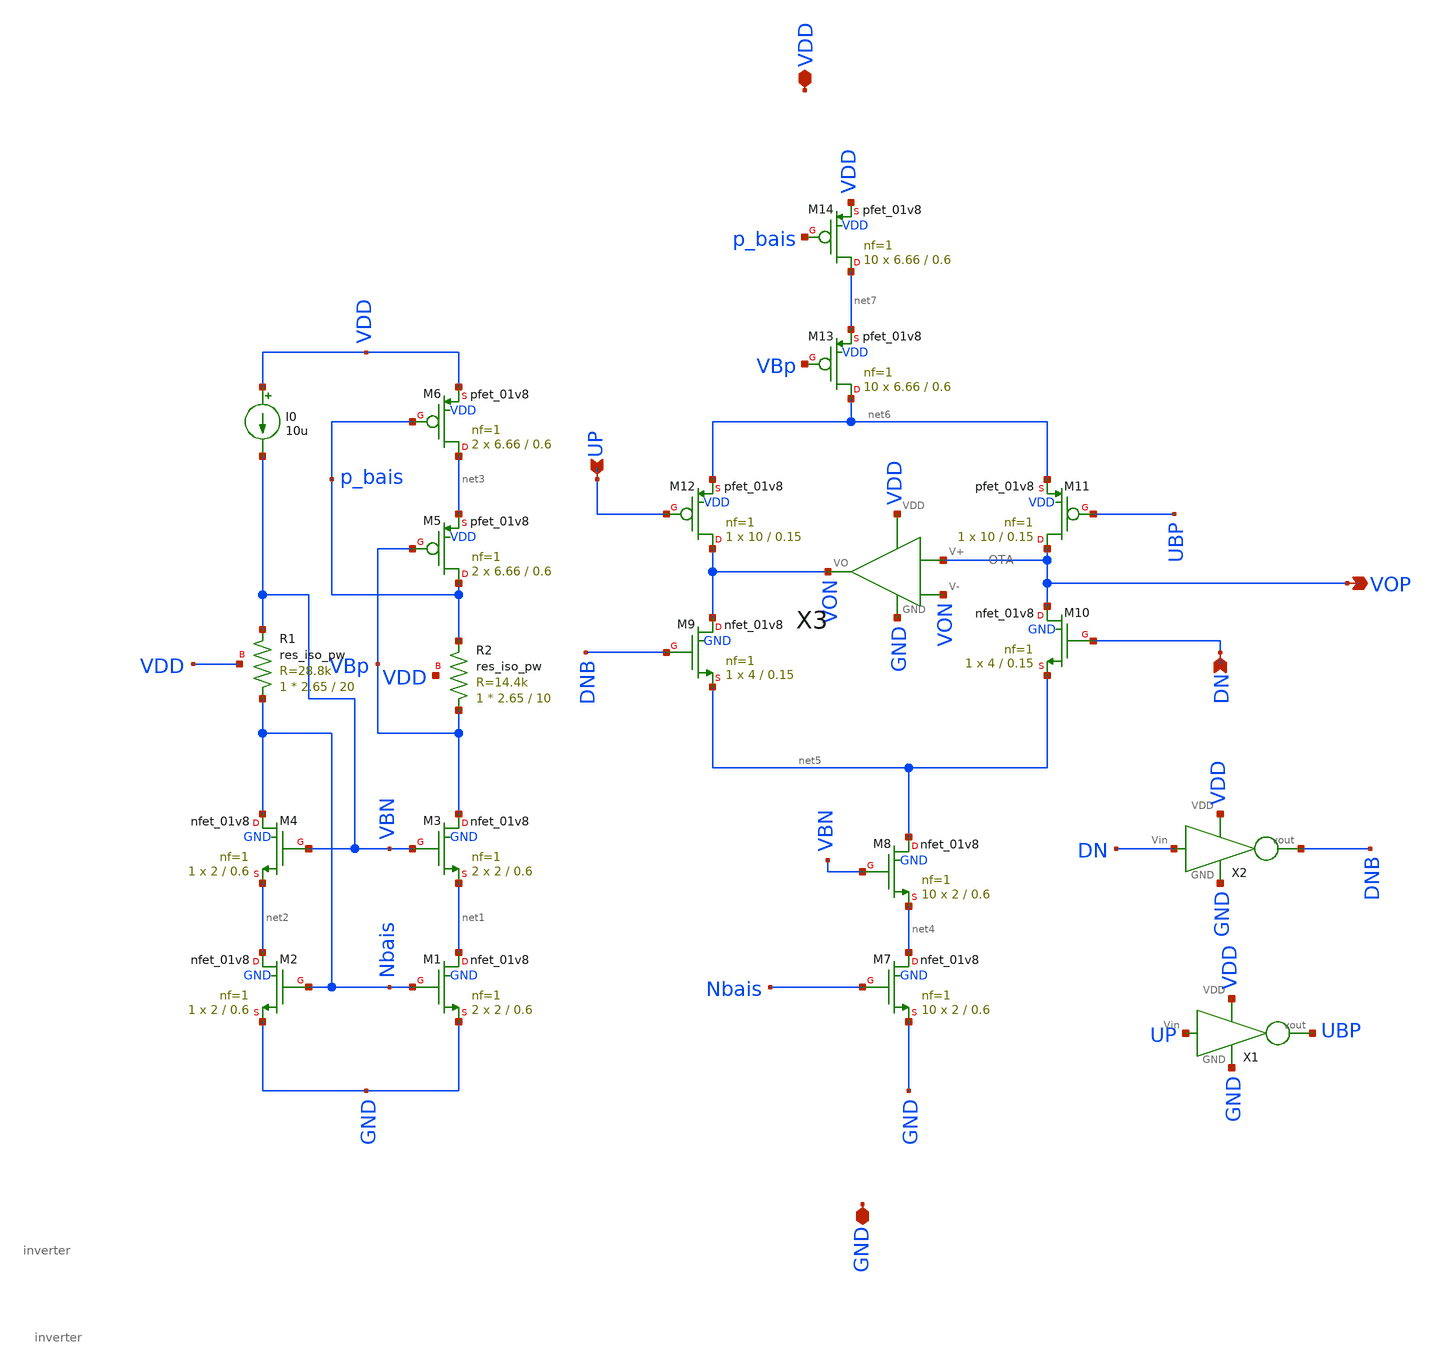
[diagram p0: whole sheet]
** sch_path: pll/pfd_cp_lf_lib/charge_pump_second_design/xschem/CP_with_buffer.sch
**.subckt CP_with_buffer VDD GND VOP DN UP
*.iopin VDD
*.iopin GND
*.opin VOP
*.ipin DN
*.ipin UP
XM1 net1 Nbais GND GND sky130_fd_pr__nfet_01v8 L=0.6 W=2 nf=1 ad='int((nf+1)/2) * W/nf * 0.29' as='int((nf+2)/2) * W/nf * 0.29'
+ pd='2*int((nf+1)/2) * (W/nf + 0.29)' ps='2*int((nf+2)/2) * (W/nf + 0.29)' nrd='0.29 / W' nrs='0.29 / W'
+ sa=0 sb=0 sd=0 mult=2 m=2
XM2 net2 Nbais GND GND sky130_fd_pr__nfet_01v8 L=0.6 W=2 nf=1 ad='int((nf+1)/2) * W/nf * 0.29' as='int((nf+2)/2) * W/nf * 0.29'
+ pd='2*int((nf+1)/2) * (W/nf + 0.29)' ps='2*int((nf+2)/2) * (W/nf + 0.29)' nrd='0.29 / W' nrs='0.29 / W'
+ sa=0 sb=0 sd=0 mult=1 m=1
XM3 VBp VBN net1 GND sky130_fd_pr__nfet_01v8 L=0.6 W=2 nf=1 ad='int((nf+1)/2) * W/nf * 0.29' as='int((nf+2)/2) * W/nf * 0.29'
+ pd='2*int((nf+1)/2) * (W/nf + 0.29)' ps='2*int((nf+2)/2) * (W/nf + 0.29)' nrd='0.29 / W' nrs='0.29 / W'
+ sa=0 sb=0 sd=0 mult=2 m=2
XM4 Nbais VBN net2 GND sky130_fd_pr__nfet_01v8 L=0.6 W=2 nf=1 ad='int((nf+1)/2) * W/nf * 0.29' as='int((nf+2)/2) * W/nf * 0.29'
+ pd='2*int((nf+1)/2) * (W/nf + 0.29)' ps='2*int((nf+2)/2) * (W/nf + 0.29)' nrd='0.29 / W' nrs='0.29 / W'
+ sa=0 sb=0 sd=0 mult=1 m=1
XM5 p_bais VBp net3 VDD sky130_fd_pr__pfet_01v8 L=0.6 W=6.66 nf=1 ad='int((nf+1)/2) * W/nf * 0.29' as='int((nf+2)/2) * W/nf * 0.29'
+ pd='2*int((nf+1)/2) * (W/nf + 0.29)' ps='2*int((nf+2)/2) * (W/nf + 0.29)' nrd='0.29 / W' nrs='0.29 / W'
+ sa=0 sb=0 sd=0 mult=2 m=2
XM6 net3 p_bais VDD VDD sky130_fd_pr__pfet_01v8 L=0.6 W=6.66 nf=1 ad='int((nf+1)/2) * W/nf * 0.29' as='int((nf+2)/2) * W/nf * 0.29'
+ pd='2*int((nf+1)/2) * (W/nf + 0.29)' ps='2*int((nf+2)/2) * (W/nf + 0.29)' nrd='0.29 / W' nrs='0.29 / W'
+ sa=0 sb=0 sd=0 mult=2 m=2
I0 VDD VBN 10u
XM7 net4 Nbais GND GND sky130_fd_pr__nfet_01v8 L=0.6 W=2 nf=1 ad='int((nf+1)/2) * W/nf * 0.29' as='int((nf+2)/2) * W/nf * 0.29'
+ pd='2*int((nf+1)/2) * (W/nf + 0.29)' ps='2*int((nf+2)/2) * (W/nf + 0.29)' nrd='0.29 / W' nrs='0.29 / W'
+ sa=0 sb=0 sd=0 mult=10 m=10
XM8 net5 VBN net4 GND sky130_fd_pr__nfet_01v8 L=0.6 W=2 nf=1 ad='int((nf+1)/2) * W/nf * 0.29' as='int((nf+2)/2) * W/nf * 0.29'
+ pd='2*int((nf+1)/2) * (W/nf + 0.29)' ps='2*int((nf+2)/2) * (W/nf + 0.29)' nrd='0.29 / W' nrs='0.29 / W'
+ sa=0 sb=0 sd=0 mult=10 m=10
XM9 VON DNB net5 GND sky130_fd_pr__nfet_01v8 L=0.15 W=4 nf=1 ad='int((nf+1)/2) * W/nf * 0.29' as='int((nf+2)/2) * W/nf * 0.29'
+ pd='2*int((nf+1)/2) * (W/nf + 0.29)' ps='2*int((nf+2)/2) * (W/nf + 0.29)' nrd='0.29 / W' nrs='0.29 / W'
+ sa=0 sb=0 sd=0 mult=1 m=1
XM10 VOP DN net5 GND sky130_fd_pr__nfet_01v8 L=0.15 W=4 nf=1 ad='int((nf+1)/2) * W/nf * 0.29' as='int((nf+2)/2) * W/nf * 0.29'
+ pd='2*int((nf+1)/2) * (W/nf + 0.29)' ps='2*int((nf+2)/2) * (W/nf + 0.29)' nrd='0.29 / W' nrs='0.29 / W'
+ sa=0 sb=0 sd=0 mult=1 m=1
XM11 VOP UBP net6 VDD sky130_fd_pr__pfet_01v8 L=0.15 W=10 nf=1 ad='int((nf+1)/2) * W/nf * 0.29' as='int((nf+2)/2) * W/nf * 0.29'
+ pd='2*int((nf+1)/2) * (W/nf + 0.29)' ps='2*int((nf+2)/2) * (W/nf + 0.29)' nrd='0.29 / W' nrs='0.29 / W'
+ sa=0 sb=0 sd=0 mult=1 m=1
XM12 VON UP net6 VDD sky130_fd_pr__pfet_01v8 L=0.15 W=10 nf=1 ad='int((nf+1)/2) * W/nf * 0.29' as='int((nf+2)/2) * W/nf * 0.29'
+ pd='2*int((nf+1)/2) * (W/nf + 0.29)' ps='2*int((nf+2)/2) * (W/nf + 0.29)' nrd='0.29 / W' nrs='0.29 / W'
+ sa=0 sb=0 sd=0 mult=1 m=1
XM13 net6 VBp net7 VDD sky130_fd_pr__pfet_01v8 L=0.6 W=6.66 nf=1 ad='int((nf+1)/2) * W/nf * 0.29' as='int((nf+2)/2) * W/nf * 0.29'
+ pd='2*int((nf+1)/2) * (W/nf + 0.29)' ps='2*int((nf+2)/2) * (W/nf + 0.29)' nrd='0.29 / W' nrs='0.29 / W'
+ sa=0 sb=0 sd=0 mult=10 m=10
XM14 net7 p_bais VDD VDD sky130_fd_pr__pfet_01v8 L=0.6 W=6.66 nf=1 ad='int((nf+1)/2) * W/nf * 0.29' as='int((nf+2)/2) * W/nf * 0.29'
+ pd='2*int((nf+1)/2) * (W/nf + 0.29)' ps='2*int((nf+2)/2) * (W/nf + 0.29)' nrd='0.29 / W' nrs='0.29 / W'
+ sa=0 sb=0 sd=0 mult=10 m=10
X1 UP UBP VDD GND inverter
X2 DN DNB VDD GND inverter
X3 VOP VON VON VDD GND OTA
XR1 Nbais VBN VDD sky130_fd_pr__res_iso_pw W=2.65 L=20 m=1
XR2 VBp p_bais VDD sky130_fd_pr__res_iso_pw W=2.65 L=10 m=1
**.ends
.end
